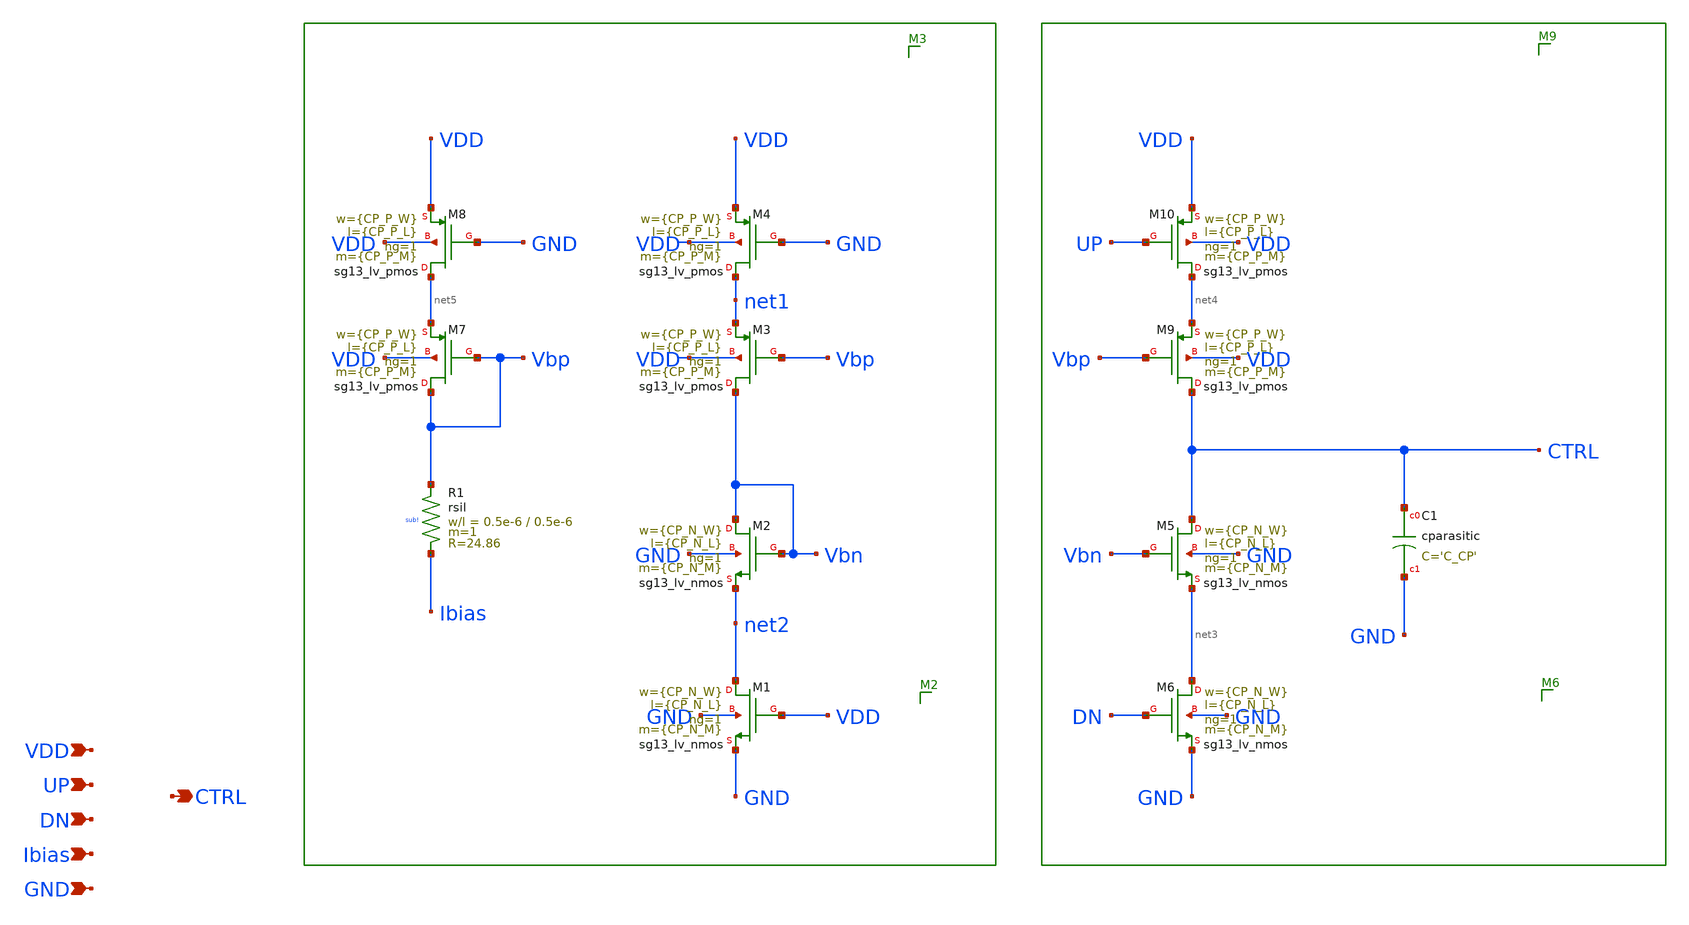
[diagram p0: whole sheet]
** sch_path: src/CP.sch
**.subckt CP CTRL UP VDD Ibias DN GND
*.opin CTRL
*.ipin UP
*.ipin VDD
*.ipin Ibias
*.ipin DN
*.ipin GND
XM2 Vbn Vbn net2 GND sg13_lv_nmos w={CP_N_W} l={CP_N_L} ng=1 m={CP_N_M} mm_ok=1
XM1 net2 VDD GND GND sg13_lv_nmos w={CP_N_W} l={CP_N_L} ng=1 m={CP_N_M} mm_ok=1
XM3 Vbn Vbp net1 VDD sg13_lv_pmos w={CP_P_W} l={CP_P_L} ng=1 m={CP_P_M} mm_ok=1
XM4 net1 GND VDD VDD sg13_lv_pmos w={CP_P_W} l={CP_P_L} ng=1 m={CP_P_M} mm_ok=1
XM7 Vbp Vbp net5 VDD sg13_lv_pmos w={CP_P_W} l={CP_P_L} ng=1 m={CP_P_M} mm_ok=1
XM8 net5 GND VDD VDD sg13_lv_pmos w={CP_P_W} l={CP_P_L} ng=1 m={CP_P_M} mm_ok=1
XM5 CTRL Vbn net3 GND sg13_lv_nmos w={CP_N_W} l={CP_N_L} ng=1 m={CP_N_M} mm_ok=1
XM6 net3 DN GND GND sg13_lv_nmos w={CP_N_W} l={CP_N_L} ng=1 m={CP_N_M} mm_ok=1
XM9 CTRL Vbp net4 VDD sg13_lv_pmos w={CP_P_W} l={CP_P_L} ng=1 m={CP_P_M} mm_ok=1
XM10 net4 UP VDD VDD sg13_lv_pmos w={CP_P_W} l={CP_P_L} ng=1 m={CP_P_M} mm_ok=1
XC1 CTRL GND cparasitic C='C_CP'
XR1 Vbp Ibias sub! rsil w=0.5e-6 l=0.5e-6 m=1 mm_ok=1
**.ends
.end
